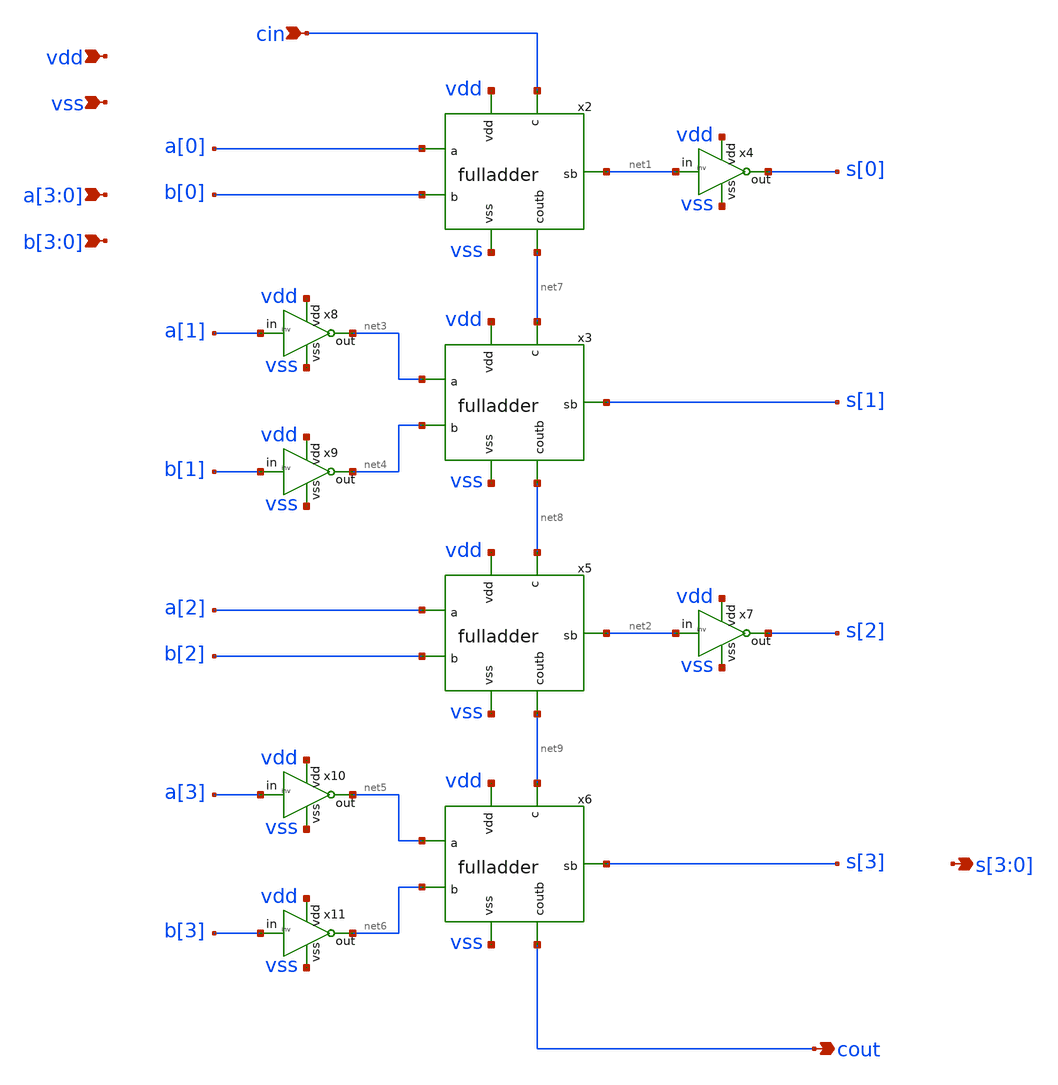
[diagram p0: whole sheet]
** sch_path: xschem/adder4.sch
**.subckt adder4 cin vdd vss a[3],a[2],a[1],a[0] b[3],b[2],b[1],b[0] cout s[3],s[2],s[1],s[0]
*.ipin cin
*.ipin vdd
*.ipin vss
*.ipin a[3],a[2],a[1],a[0]
*.ipin b[3],b[2],b[1],b[0]
*.opin cout
*.opin s[3],s[2],s[1],s[0]
x2 vdd a[0] b[0] cin net1 net7 vss fulladder
x3 vdd net3 net4 net7 s[1] net8 vss fulladder
x4 vdd net1 s[0] vss inv
x5 vdd a[2] b[2] net8 net2 net9 vss fulladder
x6 vdd net5 net6 net9 s[3] cout vss fulladder
x7 vdd net2 s[2] vss inv
x8 vdd a[1] net3 vss inv
x9 vdd b[1] net4 vss inv
x10 vdd a[3] net5 vss inv
x11 vdd b[3] net6 vss inv
**.ends

* expanding   symbol:  fulladder.sym # of pins=7
** sym_path: xschem/fulladder.sym
** sch_path: xschem/fulladder.sch
.subckt fulladder vdd a b c sb coutb vss
*.opin sb
*.opin coutb
*.ipin vss
*.ipin vdd
*.ipin a
*.ipin b
*.ipin c
XM27 net2 a vss vss nfet_03v3 L=0.28u W=0.6u nf=1 ad='int((nf+1)/2) * W/nf * 0.18u' as='int((nf+2)/2) * W/nf * 0.18u'
+ pd='2*int((nf+1)/2) * (W/nf + 0.18u)' ps='2*int((nf+2)/2) * (W/nf + 0.18u)' nrd='0.18u / W' nrs='0.18u / W'
+ sa=0 sb=0 sd=0 m=1
XM28 net1 a vdd vdd pfet_03v3 L=0.28u W=1.2u nf=1 ad='int((nf+1)/2) * W/nf * 0.18u' as='int((nf+2)/2) * W/nf * 0.18u'
+ pd='2*int((nf+1)/2) * (W/nf + 0.18u)' ps='2*int((nf+2)/2) * (W/nf + 0.18u)' nrd='0.18u / W' nrs='0.18u / W'
+ sa=0 sb=0 sd=0 m=1
XM1 net1 b vdd vdd pfet_03v3 L=0.28u W=1.2u nf=1 ad='int((nf+1)/2) * W/nf * 0.18u' as='int((nf+2)/2) * W/nf * 0.18u'
+ pd='2*int((nf+1)/2) * (W/nf + 0.18u)' ps='2*int((nf+2)/2) * (W/nf + 0.18u)' nrd='0.18u / W' nrs='0.18u / W'
+ sa=0 sb=0 sd=0 m=1
XM2 coutb c net1 vdd pfet_03v3 L=0.28u W=1.2u nf=1 ad='int((nf+1)/2) * W/nf * 0.18u' as='int((nf+2)/2) * W/nf * 0.18u'
+ pd='2*int((nf+1)/2) * (W/nf + 0.18u)' ps='2*int((nf+2)/2) * (W/nf + 0.18u)' nrd='0.18u / W' nrs='0.18u / W'
+ sa=0 sb=0 sd=0 m=1
XM3 net2 b vss vss nfet_03v3 L=0.28u W=0.6u nf=1 ad='int((nf+1)/2) * W/nf * 0.18u' as='int((nf+2)/2) * W/nf * 0.18u'
+ pd='2*int((nf+1)/2) * (W/nf + 0.18u)' ps='2*int((nf+2)/2) * (W/nf + 0.18u)' nrd='0.18u / W' nrs='0.18u / W'
+ sa=0 sb=0 sd=0 m=1
XM4 coutb c net2 vss nfet_03v3 L=0.28u W=0.6u nf=1 ad='int((nf+1)/2) * W/nf * 0.18u' as='int((nf+2)/2) * W/nf * 0.18u'
+ pd='2*int((nf+1)/2) * (W/nf + 0.18u)' ps='2*int((nf+2)/2) * (W/nf + 0.18u)' nrd='0.18u / W' nrs='0.18u / W'
+ sa=0 sb=0 sd=0 m=1
XM5 net3 b vss vss nfet_03v3 L=0.28u W=0.6u nf=1 ad='int((nf+1)/2) * W/nf * 0.18u' as='int((nf+2)/2) * W/nf * 0.18u'
+ pd='2*int((nf+1)/2) * (W/nf + 0.18u)' ps='2*int((nf+2)/2) * (W/nf + 0.18u)' nrd='0.18u / W' nrs='0.18u / W'
+ sa=0 sb=0 sd=0 m=1
XM6 coutb a net3 vss nfet_03v3 L=0.28u W=0.6u nf=1 ad='int((nf+1)/2) * W/nf * 0.18u' as='int((nf+2)/2) * W/nf * 0.18u'
+ pd='2*int((nf+1)/2) * (W/nf + 0.18u)' ps='2*int((nf+2)/2) * (W/nf + 0.18u)' nrd='0.18u / W' nrs='0.18u / W'
+ sa=0 sb=0 sd=0 m=1
XM7 net4 b vdd vdd pfet_03v3 L=0.28u W=1.2u nf=1 ad='int((nf+1)/2) * W/nf * 0.18u' as='int((nf+2)/2) * W/nf * 0.18u'
+ pd='2*int((nf+1)/2) * (W/nf + 0.18u)' ps='2*int((nf+2)/2) * (W/nf + 0.18u)' nrd='0.18u / W' nrs='0.18u / W'
+ sa=0 sb=0 sd=0 m=1
XM8 coutb a net4 vdd pfet_03v3 L=0.28u W=1.2u nf=1 ad='int((nf+1)/2) * W/nf * 0.18u' as='int((nf+2)/2) * W/nf * 0.18u'
+ pd='2*int((nf+1)/2) * (W/nf + 0.18u)' ps='2*int((nf+2)/2) * (W/nf + 0.18u)' nrd='0.18u / W' nrs='0.18u / W'
+ sa=0 sb=0 sd=0 m=1
XM9 net5 a vss vss nfet_03v3 L=0.28u W=0.6u nf=1 ad='int((nf+1)/2) * W/nf * 0.18u' as='int((nf+2)/2) * W/nf * 0.18u'
+ pd='2*int((nf+1)/2) * (W/nf + 0.18u)' ps='2*int((nf+2)/2) * (W/nf + 0.18u)' nrd='0.18u / W' nrs='0.18u / W'
+ sa=0 sb=0 sd=0 m=1
XM10 sb coutb net5 vss nfet_03v3 L=0.28u W=0.6u nf=1 ad='int((nf+1)/2) * W/nf * 0.18u' as='int((nf+2)/2) * W/nf * 0.18u'
+ pd='2*int((nf+1)/2) * (W/nf + 0.18u)' ps='2*int((nf+2)/2) * (W/nf + 0.18u)' nrd='0.18u / W' nrs='0.18u / W'
+ sa=0 sb=0 sd=0 m=1
XM11 net6 a vdd vdd pfet_03v3 L=0.28u W=1.2u nf=1 ad='int((nf+1)/2) * W/nf * 0.18u' as='int((nf+2)/2) * W/nf * 0.18u'
+ pd='2*int((nf+1)/2) * (W/nf + 0.18u)' ps='2*int((nf+2)/2) * (W/nf + 0.18u)' nrd='0.18u / W' nrs='0.18u / W'
+ sa=0 sb=0 sd=0 m=1
XM12 sb coutb net6 vdd pfet_03v3 L=0.28u W=1.2u nf=1 ad='int((nf+1)/2) * W/nf * 0.18u' as='int((nf+2)/2) * W/nf * 0.18u'
+ pd='2*int((nf+1)/2) * (W/nf + 0.18u)' ps='2*int((nf+2)/2) * (W/nf + 0.18u)' nrd='0.18u / W' nrs='0.18u / W'
+ sa=0 sb=0 sd=0 m=1
XM13 net6 b vdd vdd pfet_03v3 L=0.28u W=1.2u nf=1 ad='int((nf+1)/2) * W/nf * 0.18u' as='int((nf+2)/2) * W/nf * 0.18u'
+ pd='2*int((nf+1)/2) * (W/nf + 0.18u)' ps='2*int((nf+2)/2) * (W/nf + 0.18u)' nrd='0.18u / W' nrs='0.18u / W'
+ sa=0 sb=0 sd=0 m=1
XM14 net6 c vdd vdd pfet_03v3 L=0.28u W=1.2u nf=1 ad='int((nf+1)/2) * W/nf * 0.18u' as='int((nf+2)/2) * W/nf * 0.18u'
+ pd='2*int((nf+1)/2) * (W/nf + 0.18u)' ps='2*int((nf+2)/2) * (W/nf + 0.18u)' nrd='0.18u / W' nrs='0.18u / W'
+ sa=0 sb=0 sd=0 m=1
XM15 net5 b vss vss nfet_03v3 L=0.28u W=0.6u nf=1 ad='int((nf+1)/2) * W/nf * 0.18u' as='int((nf+2)/2) * W/nf * 0.18u'
+ pd='2*int((nf+1)/2) * (W/nf + 0.18u)' ps='2*int((nf+2)/2) * (W/nf + 0.18u)' nrd='0.18u / W' nrs='0.18u / W'
+ sa=0 sb=0 sd=0 m=1
XM16 net5 c vss vss nfet_03v3 L=0.28u W=0.6u nf=1 ad='int((nf+1)/2) * W/nf * 0.18u' as='int((nf+2)/2) * W/nf * 0.18u'
+ pd='2*int((nf+1)/2) * (W/nf + 0.18u)' ps='2*int((nf+2)/2) * (W/nf + 0.18u)' nrd='0.18u / W' nrs='0.18u / W'
+ sa=0 sb=0 sd=0 m=1
XM17 net7 c vdd vdd pfet_03v3 L=0.28u W=1.2u nf=1 ad='int((nf+1)/2) * W/nf * 0.18u' as='int((nf+2)/2) * W/nf * 0.18u'
+ pd='2*int((nf+1)/2) * (W/nf + 0.18u)' ps='2*int((nf+2)/2) * (W/nf + 0.18u)' nrd='0.18u / W' nrs='0.18u / W'
+ sa=0 sb=0 sd=0 m=1
XM18 net8 b net7 vdd pfet_03v3 L=0.28u W=1.2u nf=1 ad='int((nf+1)/2) * W/nf * 0.18u' as='int((nf+2)/2) * W/nf * 0.18u'
+ pd='2*int((nf+1)/2) * (W/nf + 0.18u)' ps='2*int((nf+2)/2) * (W/nf + 0.18u)' nrd='0.18u / W' nrs='0.18u / W'
+ sa=0 sb=0 sd=0 m=1
XM19 sb a net8 vdd pfet_03v3 L=0.28u W=1.2u nf=1 ad='int((nf+1)/2) * W/nf * 0.18u' as='int((nf+2)/2) * W/nf * 0.18u'
+ pd='2*int((nf+1)/2) * (W/nf + 0.18u)' ps='2*int((nf+2)/2) * (W/nf + 0.18u)' nrd='0.18u / W' nrs='0.18u / W'
+ sa=0 sb=0 sd=0 m=1
XM20 net9 c vss vss nfet_03v3 L=0.28u W=0.6u nf=1 ad='int((nf+1)/2) * W/nf * 0.18u' as='int((nf+2)/2) * W/nf * 0.18u'
+ pd='2*int((nf+1)/2) * (W/nf + 0.18u)' ps='2*int((nf+2)/2) * (W/nf + 0.18u)' nrd='0.18u / W' nrs='0.18u / W'
+ sa=0 sb=0 sd=0 m=1
XM21 net10 b net9 vss nfet_03v3 L=0.28u W=0.6u nf=1 ad='int((nf+1)/2) * W/nf * 0.18u' as='int((nf+2)/2) * W/nf * 0.18u'
+ pd='2*int((nf+1)/2) * (W/nf + 0.18u)' ps='2*int((nf+2)/2) * (W/nf + 0.18u)' nrd='0.18u / W' nrs='0.18u / W'
+ sa=0 sb=0 sd=0 m=1
XM22 sb a net10 vss nfet_03v3 L=0.28u W=0.6u nf=1 ad='int((nf+1)/2) * W/nf * 0.18u' as='int((nf+2)/2) * W/nf * 0.18u'
+ pd='2*int((nf+1)/2) * (W/nf + 0.18u)' ps='2*int((nf+2)/2) * (W/nf + 0.18u)' nrd='0.18u / W' nrs='0.18u / W'
+ sa=0 sb=0 sd=0 m=1
.ends


* expanding   symbol:  inv.sym # of pins=4
** sym_path: xschem/inv.sym
** sch_path: xschem/inv.sch
.subckt inv vdd in out vss
*.ipin in
*.ipin vdd
*.ipin vss
*.opin out
XM27 out in vss vss nfet_03v3 L=0.28u W=0.6u nf=1 ad='int((nf+1)/2) * W/nf * 0.18u' as='int((nf+2)/2) * W/nf * 0.18u'
+ pd='2*int((nf+1)/2) * (W/nf + 0.18u)' ps='2*int((nf+2)/2) * (W/nf + 0.18u)' nrd='0.18u / W' nrs='0.18u / W'
+ sa=0 sb=0 sd=0 m=1
XM28 out in vdd vdd pfet_03v3 L=0.28u W=1.2u nf=1 ad='int((nf+1)/2) * W/nf * 0.18u' as='int((nf+2)/2) * W/nf * 0.18u'
+ pd='2*int((nf+1)/2) * (W/nf + 0.18u)' ps='2*int((nf+2)/2) * (W/nf + 0.18u)' nrd='0.18u / W' nrs='0.18u / W'
+ sa=0 sb=0 sd=0 m=1
.ends

.end
